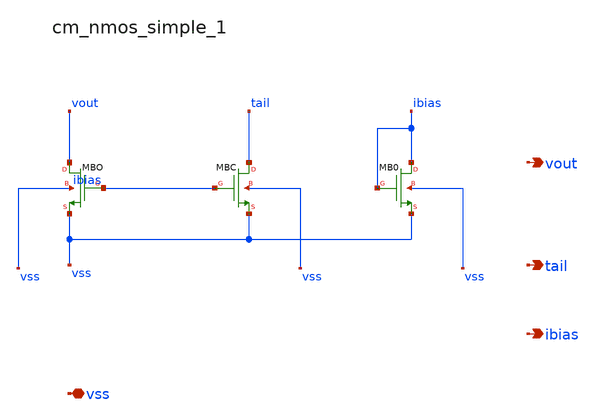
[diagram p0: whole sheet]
** sch_path: analog-db/raw/amp_033_ti_ldo_ref_selfbias/hier/blocks/cm_nmos_simple_1.sch
**.subckt cm_nmos_simple_1 vss vout tail ibias
*.iopin vss
*.opin vout
*.opin tail
*.opin ibias
XMB0 ibias ibias vss vss sg13_lv_nmos w=x_dut_xmb0_w l=x_dut_xmb0_l ng=1 m=1
XMBC tail ibias vss vss sg13_lv_nmos w=x_dut_xmbc_w l=x_dut_xmbc_l ng=1 m=x_dut_xmbc_m
XMBO vout ibias vss vss sg13_lv_nmos w=x_dut_xmbo_w l=x_dut_xmbo_l ng=1 m=x_dut_xmbo_m
**.ends
.end
